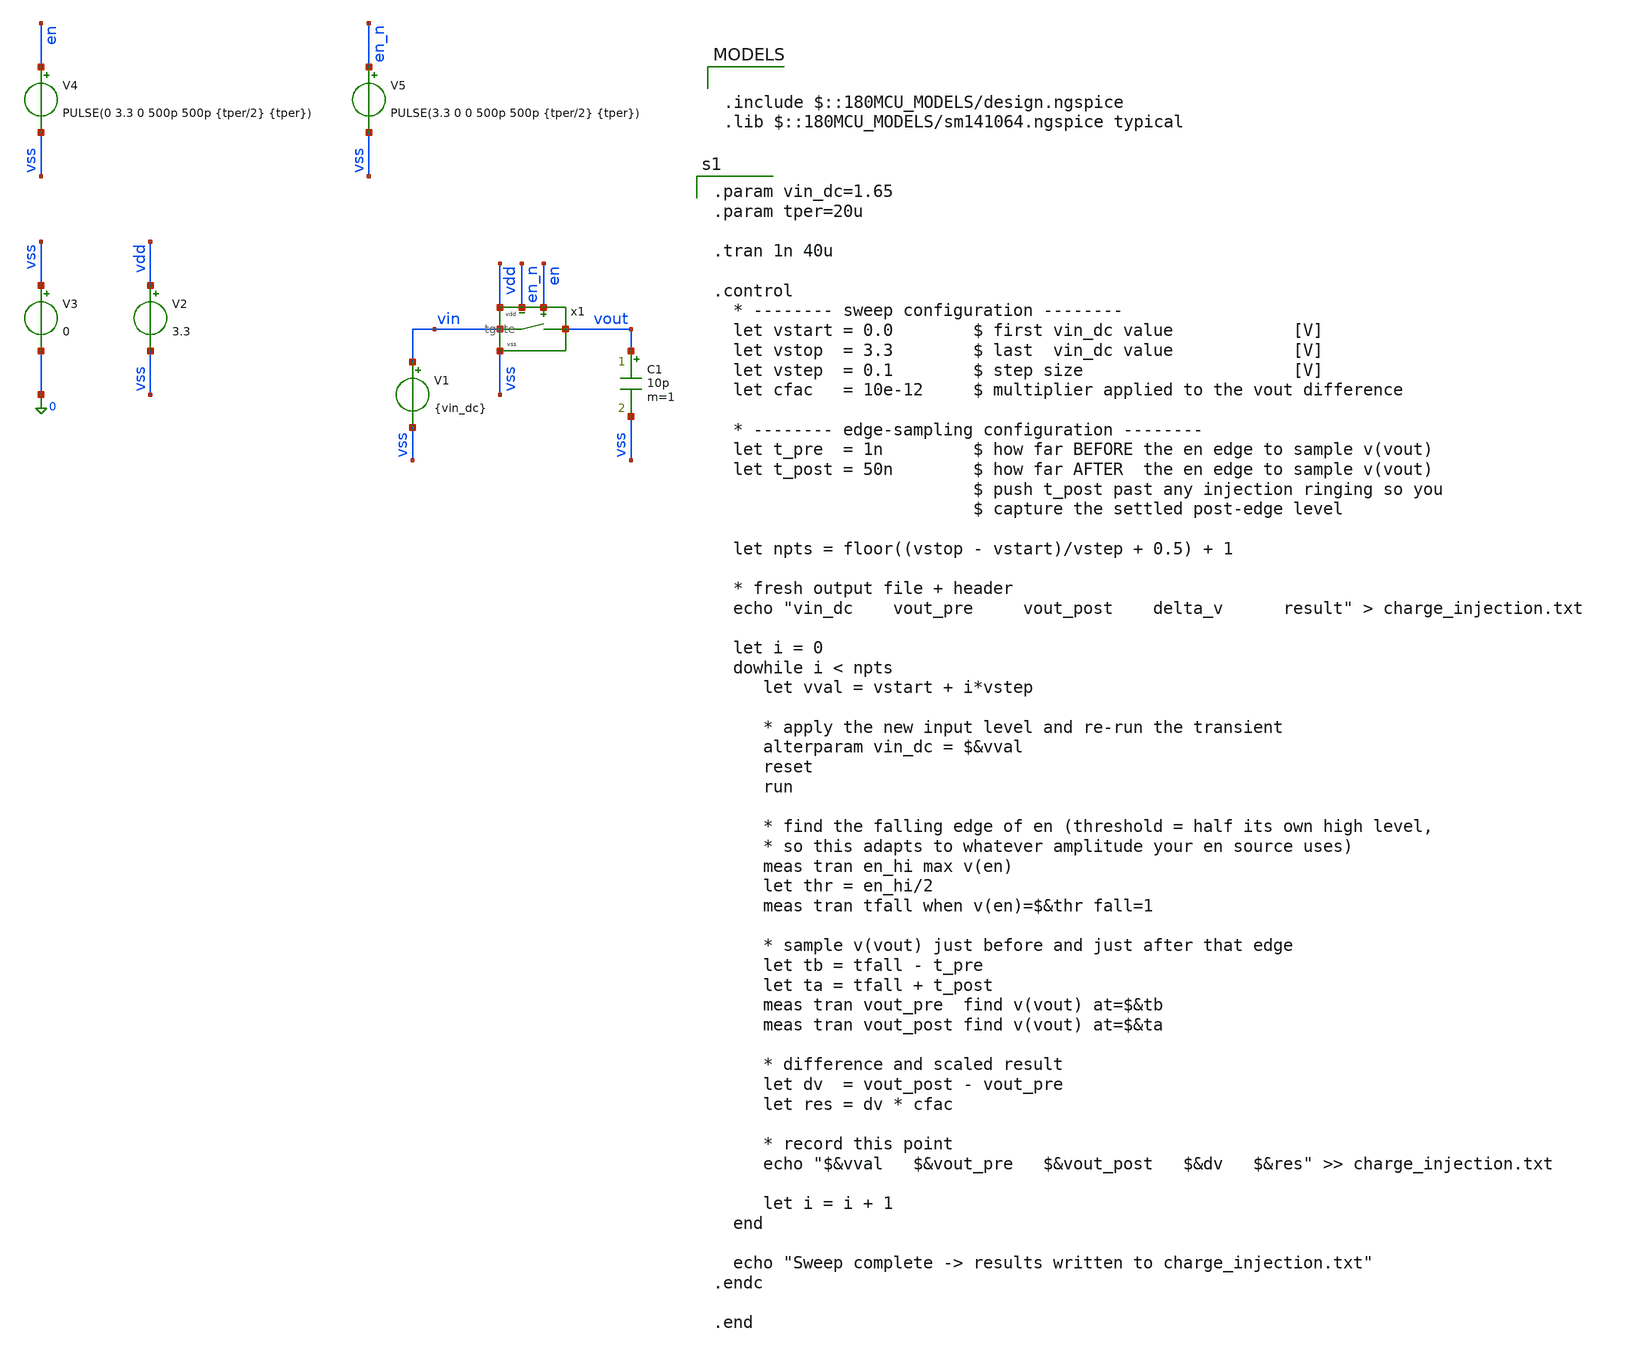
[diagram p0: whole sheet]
** sch_path: xschem/tgate/tgate_tb.sch
**.subckt tgate_tb
x1 vdd vin vss vout en_n en tgate
C1 vout vss 10p m=1
V1 vin vss {vin_dc}
V2 vdd vss 3.3
V3 vss 0 0
V4 en vss PULSE(0 3.3 0 500p 500p {tper/2} {tper})
V5 en_n vss PULSE(3.3 0 0 500p 500p {tper/2} {tper})
**** begin user architecture code

.param vin_dc=1.65
.param tper=20u

.tran 1n 40u

.control
  * -------- sweep configuration --------
  let vstart = 0.0        $ first vin_dc value            [V]
  let vstop  = 3.3        $ last  vin_dc value            [V]
  let vstep  = 0.1        $ step size                     [V]
  let cfac   = 10e-12     $ multiplier applied to the vout difference

  * -------- edge-sampling configuration --------
  let t_pre  = 1n         $ how far BEFORE the en edge to sample v(vout)
  let t_post = 50n        $ how far AFTER  the en edge to sample v(vout)
                          $ push t_post past any injection ringing so you
                          $ capture the settled post-edge level

  let npts = floor((vstop - vstart)/vstep + 0.5) + 1

  * fresh output file + header
  echo "vin_dc    vout_pre     vout_post    delta_v      result" > charge_injection.txt

  let i = 0
  dowhile i < npts
     let vval = vstart + i*vstep

     * apply the new input level and re-run the transient
     alterparam vin_dc = $&vval
     reset
     run

     * find the falling edge of en (threshold = half its own high level,
     * so this adapts to whatever amplitude your en source uses)
     meas tran en_hi max v(en)
     let thr = en_hi/2
     meas tran tfall when v(en)=$&thr fall=1

     * sample v(vout) just before and just after that edge
     let tb = tfall - t_pre
     let ta = tfall + t_post
     meas tran vout_pre  find v(vout) at=$&tb
     meas tran vout_post find v(vout) at=$&ta

     * difference and scaled result
     let dv  = vout_post - vout_pre
     let res = dv * cfac

     * record this point
     echo "$&vval   $&vout_pre   $&vout_post   $&dv   $&res" >> charge_injection.txt

     let i = i + 1
  end

  echo "Sweep complete -> results written to charge_injection.txt"
.endc

.end


.include $::180MCU_MODELS/design.ngspice
.lib $::180MCU_MODELS/sm141064.ngspice typical

**** end user architecture code
**.ends

* expanding   symbol:  tgate/tgate.sym # of pins=6
** sym_path: xschem/tgate/tgate.sym
** sch_path: xschem/tgate/tgate.sch
.subckt tgate vdd va vss vb en_n en
*.iopin vdd
*.iopin vss
*.iopin en
*.iopin va
*.iopin vb
*.iopin en_n
XM1 vb en va vss nfet_03v3 L=0.28u W=6.4u nf=4 ad='int((nf+1)/2) * W/nf * 0.18u' as='int((nf+2)/2) * W/nf * 0.18u'
+ pd='2*int((nf+1)/2) * (W/nf + 0.18u)' ps='2*int((nf+2)/2) * (W/nf + 0.18u)' nrd='0.18u / W' nrs='0.18u / W'
+ sa=0 sb=0 sd=0 m=1
XM2 va en_n vb vdd pfet_03v3 L=0.28u W=6.4u nf=4 ad='int((nf+1)/2) * W/nf * 0.18u' as='int((nf+2)/2) * W/nf * 0.18u'
+ pd='2*int((nf+1)/2) * (W/nf + 0.18u)' ps='2*int((nf+2)/2) * (W/nf + 0.18u)' nrd='0.18u / W' nrs='0.18u / W'
+ sa=0 sb=0 sd=0 m=1
.ends

.end
